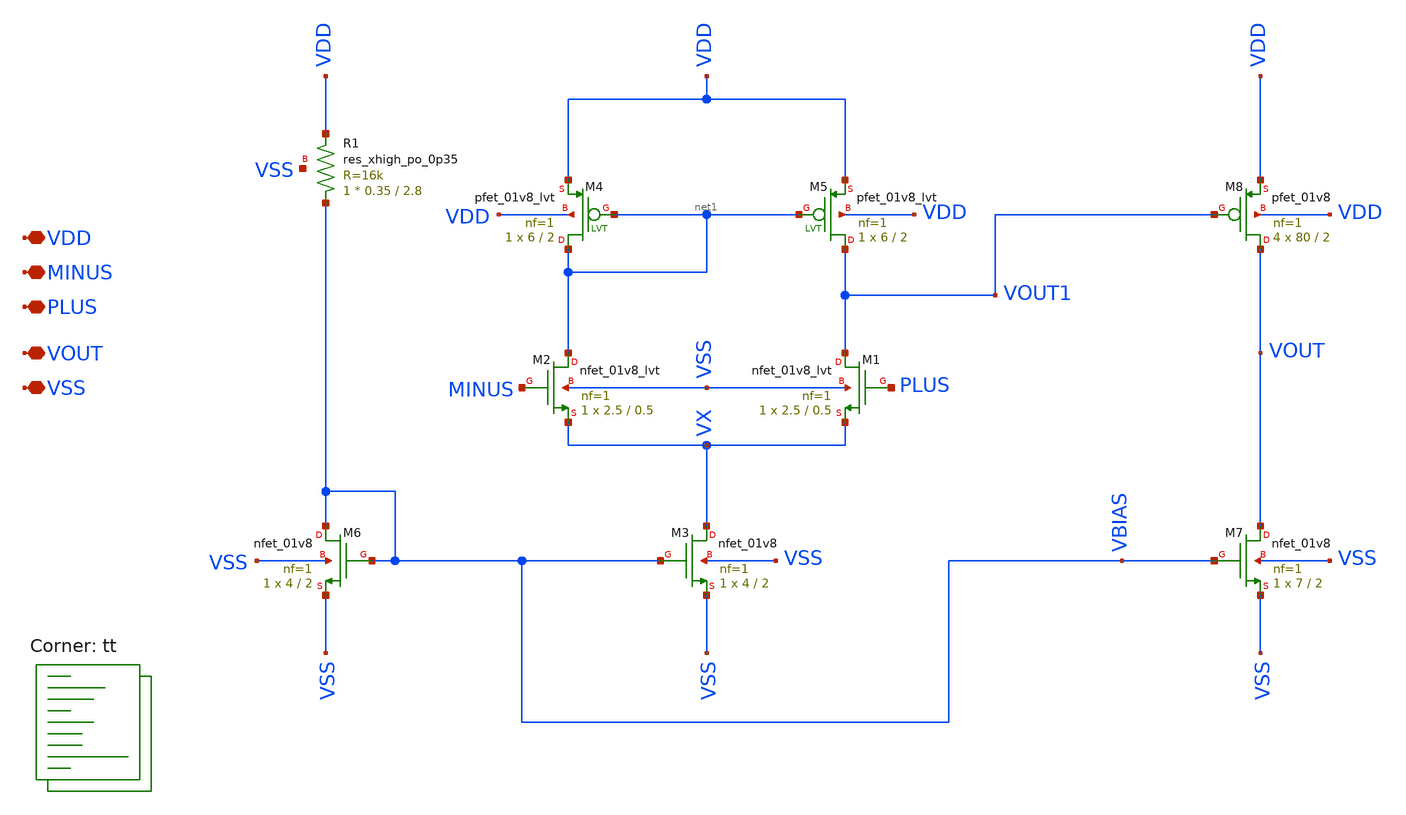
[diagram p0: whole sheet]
** sch_path: xschem/p3_opamp.sch
**.subckt p3_opamp VDD VSS PLUS MINUS VOUT
*.iopin VDD
*.iopin VSS
*.iopin PLUS
*.iopin MINUS
*.iopin VOUT
XM3 VX VBIAS VSS VSS sky130_fd_pr__nfet_01v8 L=2 W=4 nf=1 ad='int((nf+1)/2) * W/nf * 0.29' as='int((nf+2)/2) * W/nf * 0.29'
+ pd='2*int((nf+1)/2) * (W/nf + 0.29)' ps='2*int((nf+2)/2) * (W/nf + 0.29)' nrd='0.29 / W' nrs='0.29 / W'
+ sa=0 sb=0 sd=0 mult=1 m=1
XM6 VBIAS VBIAS VSS VSS sky130_fd_pr__nfet_01v8 L=2 W=4 nf=1 ad='int((nf+1)/2) * W/nf * 0.29' as='int((nf+2)/2) * W/nf * 0.29'
+ pd='2*int((nf+1)/2) * (W/nf + 0.29)' ps='2*int((nf+2)/2) * (W/nf + 0.29)' nrd='0.29 / W' nrs='0.29 / W'
+ sa=0 sb=0 sd=0 mult=1 m=1
XM7 VOUT VBIAS VSS VSS sky130_fd_pr__nfet_01v8 L=2 W=7 nf=1 ad='int((nf+1)/2) * W/nf * 0.29' as='int((nf+2)/2) * W/nf * 0.29'
+ pd='2*int((nf+1)/2) * (W/nf + 0.29)' ps='2*int((nf+2)/2) * (W/nf + 0.29)' nrd='0.29 / W' nrs='0.29 / W'
+ sa=0 sb=0 sd=0 mult=1 m=1
XM8 VOUT VOUT1 VDD VDD sky130_fd_pr__pfet_01v8 L=2 W=80 nf=1 ad='int((nf+1)/2) * W/nf * 0.29' as='int((nf+2)/2) * W/nf * 0.29'
+ pd='2*int((nf+1)/2) * (W/nf + 0.29)' ps='2*int((nf+2)/2) * (W/nf + 0.29)' nrd='0.29 / W' nrs='0.29 / W'
+ sa=0 sb=0 sd=0 mult=4 m=4
XR1 VBIAS VDD VSS sky130_fd_pr__res_xhigh_po_0p35 L=2.8 mult=1 m=1
XM2 net1 MINUS VX VSS sky130_fd_pr__nfet_01v8_lvt L=0.5 W=2.5 nf=1 ad='int((nf+1)/2) * W/nf * 0.29' as='int((nf+2)/2) * W/nf * 0.29'
+ pd='2*int((nf+1)/2) * (W/nf + 0.29)' ps='2*int((nf+2)/2) * (W/nf + 0.29)' nrd='0.29 / W' nrs='0.29 / W'
+ sa=0 sb=0 sd=0 mult=1 m=1
XM1 VOUT1 PLUS VX VSS sky130_fd_pr__nfet_01v8_lvt L=0.5 W=2.5 nf=1 ad='int((nf+1)/2) * W/nf * 0.29' as='int((nf+2)/2) * W/nf * 0.29'
+ pd='2*int((nf+1)/2) * (W/nf + 0.29)' ps='2*int((nf+2)/2) * (W/nf + 0.29)' nrd='0.29 / W' nrs='0.29 / W'
+ sa=0 sb=0 sd=0 mult=1 m=1
XM4 net1 net1 VDD VDD sky130_fd_pr__pfet_01v8_lvt L=2 W=6 nf=1 ad='int((nf+1)/2) * W/nf * 0.29' as='int((nf+2)/2) * W/nf * 0.29'
+ pd='2*int((nf+1)/2) * (W/nf + 0.29)' ps='2*int((nf+2)/2) * (W/nf + 0.29)' nrd='0.29 / W' nrs='0.29 / W'
+ sa=0 sb=0 sd=0 mult=1 m=1
XM5 VOUT1 net1 VDD VDD sky130_fd_pr__pfet_01v8_lvt L=2 W=6 nf=1 ad='int((nf+1)/2) * W/nf * 0.29' as='int((nf+2)/2) * W/nf * 0.29'
+ pd='2*int((nf+1)/2) * (W/nf + 0.29)' ps='2*int((nf+2)/2) * (W/nf + 0.29)' nrd='0.29 / W' nrs='0.29 / W'
+ sa=0 sb=0 sd=0 mult=1 m=1
**** begin user architecture code
.lib $::SKYWATER_MODELS/sky130.lib.spice tt
**** end user architecture code
**.ends
.end
